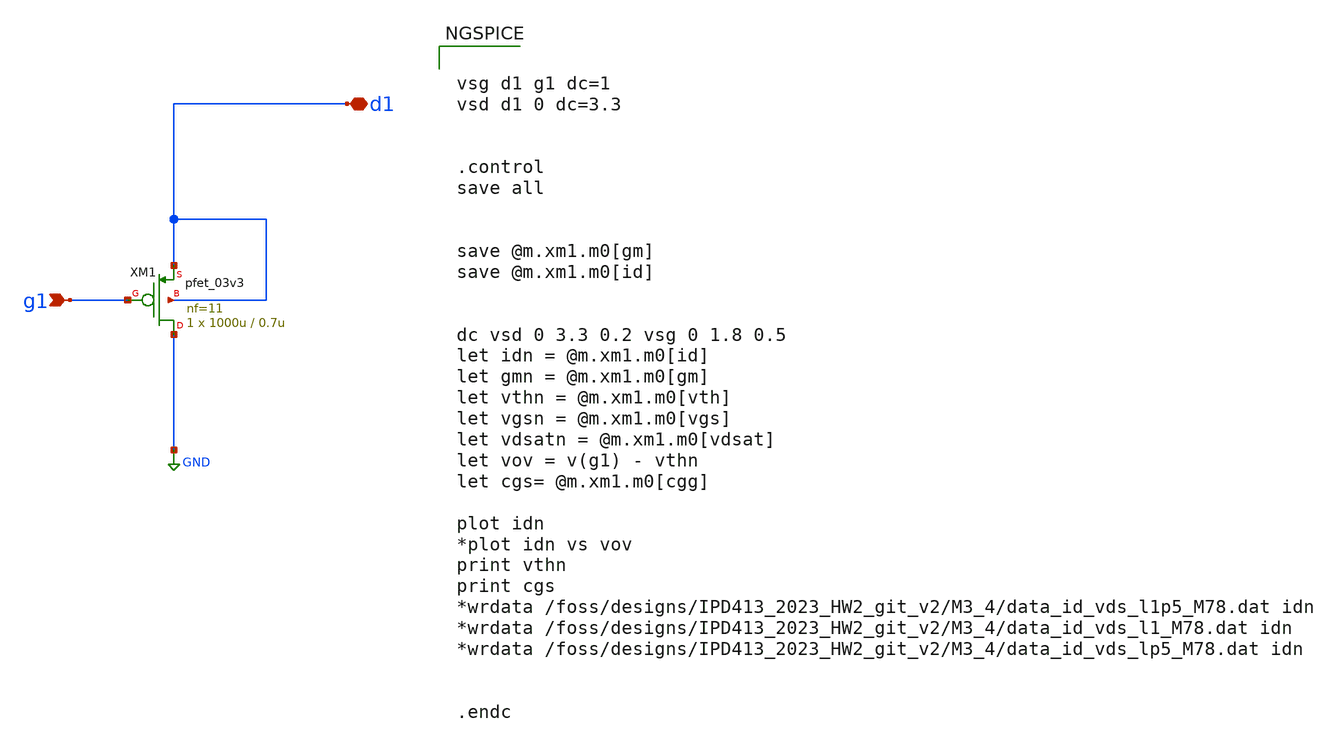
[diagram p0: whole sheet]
** sch_path: LDO/xschem/Caracteristica_disp/pmos_gf180_3p3V.sch

.include $env(PDK_ROOT)/$env(PDK)/libs.tech/ngspice/design.ngspice

.lib $env(PDK_ROOT)/$env(PDK)/libs.tech/ngspice/sm141064.ngspice typical
.lib $env(PDK_ROOT)/$env(PDK)/libs.tech/ngspice/sm141064.ngspice mimcap_statistical
.lib $env(PDK_ROOT)/$env(PDK)/libs.tech/ngspice/sm141064.ngspice cap_mim
.lib $env(PDK_ROOT)/$env(PDK)/libs.tech/ngspice/sm141064.ngspice res_typical
.lib $env(PDK_ROOT)/$env(PDK)/libs.tech/ngspice/sm141064.ngspice bjt_typical
.lib $env(PDK_ROOT)/$env(PDK)/libs.tech/ngspice/sm141064.ngspice moscap_typical


**.subckt pmos_gf180_3p3V g1 d1
*.ipin g1
*.iopin d1
XM1 GND g1 d1 d1 pfet_03v3 L=0.7u W=1000u nf=11 ad='int((nf+1)/2) * W/nf * 0.18u' as='int((nf+2)/2) * W/nf * 0.18u'
+ pd='2*int((nf+1)/2) * (W/nf + 0.18u)' ps='2*int((nf+2)/2) * (W/nf + 0.18u)' nrd='0.18u / W' nrs='0.18u / W'
+ sa=0 sb=0 sd=0 m=1
**** begin user architecture code


vsg d1 g1 dc=1
vsd d1 0 dc=3.3


.control
save all


save @m.xm1.m0[gm]
save @m.xm1.m0[id]


dc vsd 0 3.3 0.2 vsg 0 1.8 0.5
let idn = @m.xm1.m0[id]
let gmn = @m.xm1.m0[gm]
let vthn = @m.xm1.m0[vth]
let vgsn = @m.xm1.m0[vgs]
let vdsatn = @m.xm1.m0[vdsat]
let vov = v(g1) - vthn
let cgs= @m.xm1.m0[cgg]

plot idn
*plot idn vs vov
print vthn
print cgs
*wrdata /foss/designs/IPD413_2023_HW2_git_v2/M3_4/data_id_vds_l1p5_M78.dat idn
*wrdata /foss/designs/IPD413_2023_HW2_git_v2/M3_4/data_id_vds_l1_M78.dat idn
*wrdata /foss/designs/IPD413_2023_HW2_git_v2/M3_4/data_id_vds_lp5_M78.dat idn


.endc


**** end user architecture code
**.ends
.GLOBAL GND
.end
